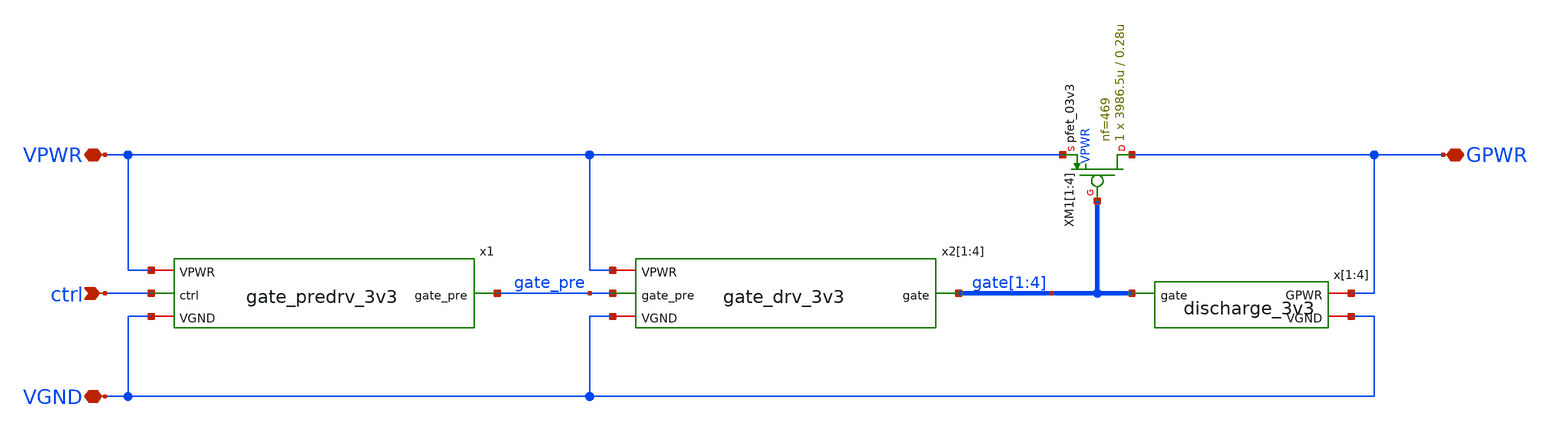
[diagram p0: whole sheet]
** sch_path: pg/gf180mcuD/tt_pg_3v3_hp_8/xschem/tt_pg_3v3_hp_8.sch
**.subckt tt_pg_3v3_hp_8 ctrl VPWR VGND GPWR
*.ipin ctrl
*.iopin VPWR
*.iopin VGND
*.iopin GPWR
x[1] VGND GPWR gate[1] discharge_3v3
x[2] VGND GPWR gate[2] discharge_3v3
x[3] VGND GPWR gate[3] discharge_3v3
x[4] VGND GPWR gate[4] discharge_3v3
XM1[1] GPWR gate[1] VPWR VPWR pfet_03v3 L=0.28u W=3986.5u nf=469 ad='int((nf+1)/2) * W/nf * 0.18u' as='int((nf+2)/2) * W/nf * 0.18u'
+ pd='2*int((nf+1)/2) * (W/nf + 0.18u)' ps='2*int((nf+2)/2) * (W/nf + 0.18u)' nrd='0.18u / W' nrs='0.18u / W'
+ sa=0 sb=0 sd=0 m=1 par=1
XM1[2] GPWR gate[2] VPWR VPWR pfet_03v3 L=0.28u W=3986.5u nf=469 ad='int((nf+1)/2) * W/nf * 0.18u' as='int((nf+2)/2) * W/nf * 0.18u'
+ pd='2*int((nf+1)/2) * (W/nf + 0.18u)' ps='2*int((nf+2)/2) * (W/nf + 0.18u)' nrd='0.18u / W' nrs='0.18u / W'
+ sa=0 sb=0 sd=0 m=1 par=1
XM1[3] GPWR gate[3] VPWR VPWR pfet_03v3 L=0.28u W=3986.5u nf=469 ad='int((nf+1)/2) * W/nf * 0.18u' as='int((nf+2)/2) * W/nf * 0.18u'
+ pd='2*int((nf+1)/2) * (W/nf + 0.18u)' ps='2*int((nf+2)/2) * (W/nf + 0.18u)' nrd='0.18u / W' nrs='0.18u / W'
+ sa=0 sb=0 sd=0 m=1 par=1
XM1[4] GPWR gate[4] VPWR VPWR pfet_03v3 L=0.28u W=3986.5u nf=469 ad='int((nf+1)/2) * W/nf * 0.18u' as='int((nf+2)/2) * W/nf * 0.18u'
+ pd='2*int((nf+1)/2) * (W/nf + 0.18u)' ps='2*int((nf+2)/2) * (W/nf + 0.18u)' nrd='0.18u / W' nrs='0.18u / W'
+ sa=0 sb=0 sd=0 m=1 par=1
x1 VGND VPWR ctrl gate_pre gate_predrv_3v3
x2[1] VGND VPWR gate_pre gate[1] gate_drv_3v3
x2[2] VGND VPWR gate_pre gate[2] gate_drv_3v3
x2[3] VGND VPWR gate_pre gate[3] gate_drv_3v3
x2[4] VGND VPWR gate_pre gate[4] gate_drv_3v3
**.ends

* expanding   symbol:  discharge_3v3.sym # of pins=3
** sym_path: pg/gf180mcuD/common/xschem/discharge_3v3.sym
** sch_path: pg/gf180mcuD/common/xschem/discharge_3v3.sch
.subckt discharge_3v3 VGND GPWR gate
*.iopin GPWR
*.iopin VGND
*.ipin gate
XM1 GPWR gate net3 VGND nfet_03v3 L=0.6u W=0.99u nf=1 ad='int((nf+1)/2) * W/nf * 0.18u' as='int((nf+2)/2) * W/nf * 0.18u'
+ pd='2*int((nf+1)/2) * (W/nf + 0.18u)' ps='2*int((nf+2)/2) * (W/nf + 0.18u)' nrd='0.18u / W' nrs='0.18u / W'
+ sa=0 sb=0 sd=0 m=1 par=1
XM2 net3 gate net2 VGND nfet_03v3 L=0.6u W=0.99u nf=1 ad='int((nf+1)/2) * W/nf * 0.18u' as='int((nf+2)/2) * W/nf * 0.18u'
+ pd='2*int((nf+1)/2) * (W/nf + 0.18u)' ps='2*int((nf+2)/2) * (W/nf + 0.18u)' nrd='0.18u / W' nrs='0.18u / W'
+ sa=0 sb=0 sd=0 m=1 par=1
XM3 net2 gate net1 VGND nfet_03v3 L=0.6u W=0.99u nf=1 ad='int((nf+1)/2) * W/nf * 0.18u' as='int((nf+2)/2) * W/nf * 0.18u'
+ pd='2*int((nf+1)/2) * (W/nf + 0.18u)' ps='2*int((nf+2)/2) * (W/nf + 0.18u)' nrd='0.18u / W' nrs='0.18u / W'
+ sa=0 sb=0 sd=0 m=1 par=1
XM4 net1 gate VGND VGND nfet_03v3 L=0.6u W=0.99u nf=1 ad='int((nf+1)/2) * W/nf * 0.18u' as='int((nf+2)/2) * W/nf * 0.18u'
+ pd='2*int((nf+1)/2) * (W/nf + 0.18u)' ps='2*int((nf+2)/2) * (W/nf + 0.18u)' nrd='0.18u / W' nrs='0.18u / W'
+ sa=0 sb=0 sd=0 m=1 par=1
XM5 GPWR gate net6 VGND nfet_03v3 L=0.6u W=0.99u nf=1 ad='int((nf+1)/2) * W/nf * 0.18u' as='int((nf+2)/2) * W/nf * 0.18u'
+ pd='2*int((nf+1)/2) * (W/nf + 0.18u)' ps='2*int((nf+2)/2) * (W/nf + 0.18u)' nrd='0.18u / W' nrs='0.18u / W'
+ sa=0 sb=0 sd=0 m=1 par=1
XM6 net6 gate net5 VGND nfet_03v3 L=0.6u W=0.99u nf=1 ad='int((nf+1)/2) * W/nf * 0.18u' as='int((nf+2)/2) * W/nf * 0.18u'
+ pd='2*int((nf+1)/2) * (W/nf + 0.18u)' ps='2*int((nf+2)/2) * (W/nf + 0.18u)' nrd='0.18u / W' nrs='0.18u / W'
+ sa=0 sb=0 sd=0 m=1 par=1
XM7 net5 gate net4 VGND nfet_03v3 L=0.6u W=0.99u nf=1 ad='int((nf+1)/2) * W/nf * 0.18u' as='int((nf+2)/2) * W/nf * 0.18u'
+ pd='2*int((nf+1)/2) * (W/nf + 0.18u)' ps='2*int((nf+2)/2) * (W/nf + 0.18u)' nrd='0.18u / W' nrs='0.18u / W'
+ sa=0 sb=0 sd=0 m=1 par=1
XM8 net4 gate VGND VGND nfet_03v3 L=0.6u W=0.99u nf=1 ad='int((nf+1)/2) * W/nf * 0.18u' as='int((nf+2)/2) * W/nf * 0.18u'
+ pd='2*int((nf+1)/2) * (W/nf + 0.18u)' ps='2*int((nf+2)/2) * (W/nf + 0.18u)' nrd='0.18u / W' nrs='0.18u / W'
+ sa=0 sb=0 sd=0 m=1 par=1
.ends


* expanding   symbol:  gate_predrv_3v3.sym # of pins=4
** sym_path: pg/gf180mcuD/common/xschem/gate_predrv_3v3.sym
** sch_path: pg/gf180mcuD/common/xschem/gate_predrv_3v3.sch
.subckt gate_predrv_3v3 VGND VPWR ctrl gate_pre
*.iopin VPWR
*.iopin VGND
*.ipin ctrl
*.opin gate_pre
XM1 gate_pre ctrl VGND VGND nfet_03v3 L=0.28u W=5.5u nf=4 ad='int((nf+1)/2) * W/nf * 0.18u' as='int((nf+2)/2) * W/nf * 0.18u'
+ pd='2*int((nf+1)/2) * (W/nf + 0.18u)' ps='2*int((nf+2)/2) * (W/nf + 0.18u)' nrd='0.18u / W' nrs='0.18u / W'
+ sa=0 sb=0 sd=0 m=1 par=1
XM2 gate_pre ctrl VPWR VPWR pfet_03v3 L=0.28u W=10.34u nf=2 ad='int((nf+1)/2) * W/nf * 0.18u' as='int((nf+2)/2) * W/nf * 0.18u'
+ pd='2*int((nf+1)/2) * (W/nf + 0.18u)' ps='2*int((nf+2)/2) * (W/nf + 0.18u)' nrd='0.18u / W' nrs='0.18u / W'
+ sa=0 sb=0 sd=0 m=1 par=1
.ends


* expanding   symbol:  gate_drv_3v3.sym # of pins=4
** sym_path: pg/gf180mcuD/common/xschem/gate_drv_3v3.sym
** sch_path: pg/gf180mcuD/common/xschem/gate_drv_3v3.sch
.subckt gate_drv_3v3 VGND VPWR gate_pre gate
*.iopin VPWR
*.iopin VGND
*.ipin gate_pre
*.opin gate
XM1 net1 gate_pre VGND VGND nfet_03v3 L=0.28u W=2.75u nf=4 ad='int((nf+1)/2) * W/nf * 0.18u' as='int((nf+2)/2) * W/nf * 0.18u'
+ pd='2*int((nf+1)/2) * (W/nf + 0.18u)' ps='2*int((nf+2)/2) * (W/nf + 0.18u)' nrd='0.18u / W' nrs='0.18u / W'
+ sa=0 sb=0 sd=0 m=1 par=1
XM2 net1 gate_pre VPWR VPWR pfet_03v3 L=0.28u W=5.17u nf=1 ad='int((nf+1)/2) * W/nf * 0.18u' as='int((nf+2)/2) * W/nf * 0.18u'
+ pd='2*int((nf+1)/2) * (W/nf + 0.18u)' ps='2*int((nf+2)/2) * (W/nf + 0.18u)' nrd='0.18u / W' nrs='0.18u / W'
+ sa=0 sb=0 sd=0 m=1 par=1
XM3 gate net1 VGND VGND nfet_03v3 L=0.28u W=11.0u nf=4 ad='int((nf+1)/2) * W/nf * 0.18u' as='int((nf+2)/2) * W/nf * 0.18u'
+ pd='2*int((nf+1)/2) * (W/nf + 0.18u)' ps='2*int((nf+2)/2) * (W/nf + 0.18u)' nrd='0.18u / W' nrs='0.18u / W'
+ sa=0 sb=0 sd=0 m=1 par=1
XM4 gate net1 VPWR VPWR pfet_03v3 L=0.28u W=20.68u nf=4 ad='int((nf+1)/2) * W/nf * 0.18u' as='int((nf+2)/2) * W/nf * 0.18u'
+ pd='2*int((nf+1)/2) * (W/nf + 0.18u)' ps='2*int((nf+2)/2) * (W/nf + 0.18u)' nrd='0.18u / W' nrs='0.18u / W'
+ sa=0 sb=0 sd=0 m=1 par=1
.ends

.end
